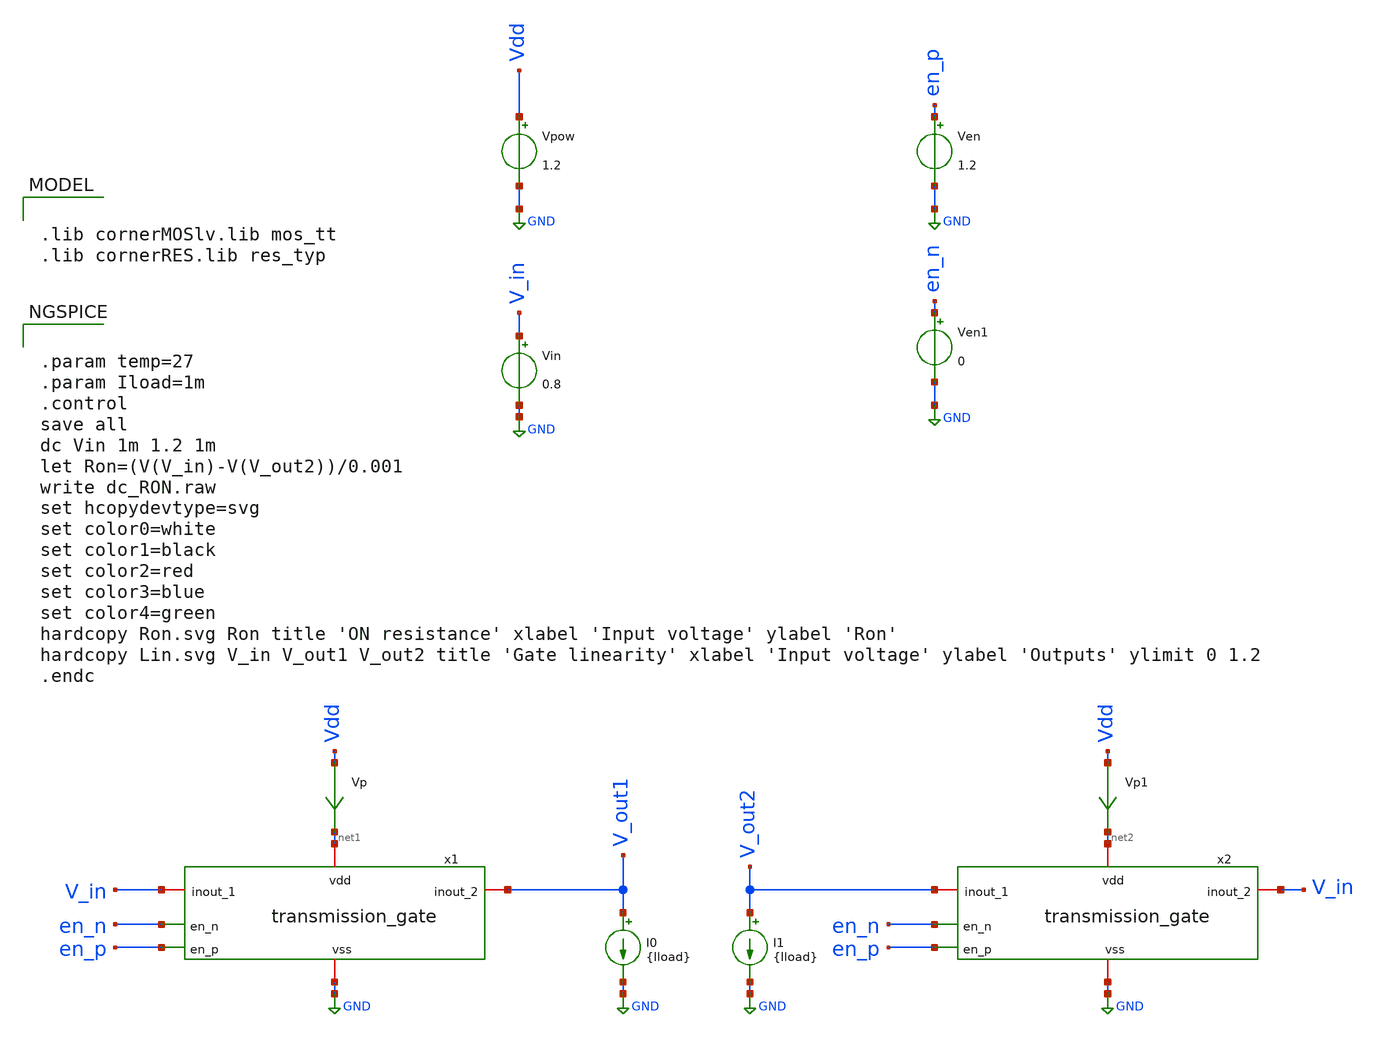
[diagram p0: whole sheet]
** sch_path: CHIPCHILE_CANELOS24_WorkshopTO/design_data/xschem/tgate/transmission_gate_tb_RON.sch
* Copyright 2023 IHP PDK Authors
**.subckt transmission_gate_tb_RON
Vpow Vdd GND 1.2
Vp Vdd net1 0
.save i(vp)
Vin V_in GND 0.8
Ven en_p GND 1.2
Ven1 en_n GND 0
x1 net1 en_n V_in V_out1 en_p GND transmission_gate
I0 V_out1 GND {Iload}
Vp1 Vdd net2 0
.save i(vp1)
x2 net2 en_n V_out2 V_in en_p GND transmission_gate
I1 V_out2 GND {Iload}
**** begin user architecture code

.lib cornerMOSlv.lib mos_tt
.lib cornerRES.lib res_typ



.param temp=27
.param Iload=1m
.control
save all
dc Vin 1m 1.2 1m
let Ron=(V(V_in)-V(V_out2))/0.001
write dc_RON.raw
set hcopydevtype=svg
set color0=white
set color1=black
set color2=red
set color3=blue
set color4=green
hardcopy Ron.svg Ron title 'ON resistance' xlabel 'Input voltage' ylabel 'Ron'
hardcopy Lin.svg V_in V_out1 V_out2 title 'Gate linearity' xlabel 'Input voltage' ylabel 'Outputs' ylimit
+ 0 1.2
.endc


**** end user architecture code
**.ends

* expanding   symbol:  transmission_gate.sym # of pins=6
** sym_path: CHIPCHILE_CANELOS24_WorkshopTO/design_data/xschem/multiplexer/transmission_gate.sym
** sch_path: CHIPCHILE_CANELOS24_WorkshopTO/design_data/xschem/multiplexer/transmission_gate.sch
.subckt transmission_gate vdd en_n inout_1 inout_2 en_p vss
*.iopin inout_1
*.iopin inout_2
*.ipin en_p
*.iopin vdd
*.iopin vss
*.ipin en_n
XM1 inout_1 en_p inout_2 net1 sg13_lv_nmos w=200.0u l=0.130u ng=20 m=1 mm_ok=1
XM2 inout_1 en_n inout_2 net2 sg13_lv_pmos w=200.0u l=0.130u ng=20 m=1 mm_ok=1
XR1 vdd net2 ntap1 R=262.8 w=0.78e-6 l=0.78e-6
XR2 vss net1 ptap1 R=262.8 w=0.78e-6 l=0.78e-6
.ends

.GLOBAL GND
.end
